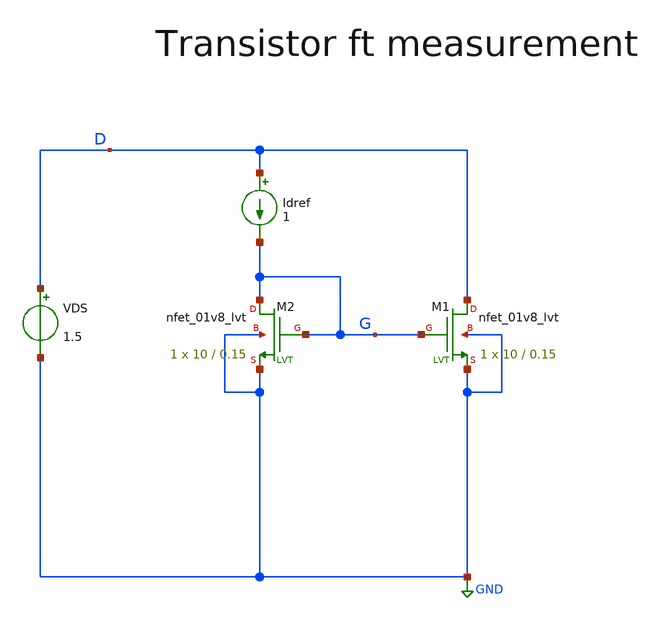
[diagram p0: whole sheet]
** sch_path: sky130_tests/tb_ft_test.sch
**.subckt tb_ft_test
XM1 D G GND GND sky130_fd_pr__nfet_01v8_lvt W=10 L=0.15 ad='int((nf+1)/2) * W/nf * 0.29' pd='2*int((nf+1)/2) * (W/nf + 0.29)'
+ as='int((nf+2)/2) * W/nf * 0.29' ps='2*int((nf+2)/2) * (W/nf + 0.29)' nrd='0.29 / W' nrs='0.29 / W' sa=0
+ sb=0 sd=0 nf=1 mult=1 m=1
VDS D GND 1.5
Idref D G 1
XM2 G G GND GND sky130_fd_pr__nfet_01v8_lvt W=10 L=0.15 ad='int((nf+1)/2) * W/nf * 0.29' pd='2*int((nf+1)/2) * (W/nf + 0.29)'
+ as='int((nf+2)/2) * W/nf * 0.29' ps='2*int((nf+2)/2) * (W/nf + 0.29)' nrd='0.29 / W' nrs='0.29 / W' sa=0
+ sb=0 sd=0 nf=1 mult=1 m=1
**** begin user architecture code



.options filetype=ascii
.save all

.op
.control
*dc Idref 0.1e-3 10e-3 0.1e-3

let n_idx = 101

let start_iref = 0.1e-3
let stop_iref = 10e-3
let delta_iref = (stop_iref - start_iref) / n_idx
let iref_act = start_iref

let vgs = unitvec(n_idx)
let gms = unitvec(n_idx)
let ids = unitvec(n_idx)

let cgss = unitvec(n_idx)
let cgds = unitvec(n_idx)

let idxs = 0
let idx = idxs

*loop
while iref_act le stop_iref
  alter idref iref_act
  run
  *print @m.xm2.msky130_fd_pr__nfet_01v8_lvt[gm]

  let gms[idx] = @m.xm2.msky130_fd_pr__nfet_01v8_lvt[gm]
  let ids[idx] = @m.xm2.msky130_fd_pr__nfet_01v8_lvt[id]

  let cgss[idx] = @m.xm2.msky130_fd_pr__nfet_01v8_lvt[cgs]
  let cgds[idx] = @m.xm2.msky130_fd_pr__nfet_01v8_lvt[cgd]
  let vgs[idx] = v(G)

  let iref_act = iref_act + delta_iref
  let idxs = idx + 1
  let idx = idxs
end

let ft = -gms/(2*pi*(cgss+cgds))
settype voltage vgs
settype current ids
setscale ids
plot gms vs ids
plot xlog ft vs ids
plot xlog vgs vs ids

.endc
.end


 ** manual skywater pdks install (with patches applied)
* .lib $::SKYWATER_MODELS/models/sky130.lib.spice tt

** opencircuitdesign pdks install
.lib $::SKYWATER_MODELS/sky130.lib.spice tt

.param mc_mm_switch=0
.param mc_pr_switch=0

**** end user architecture code
**.ends
.GLOBAL GND
.end
